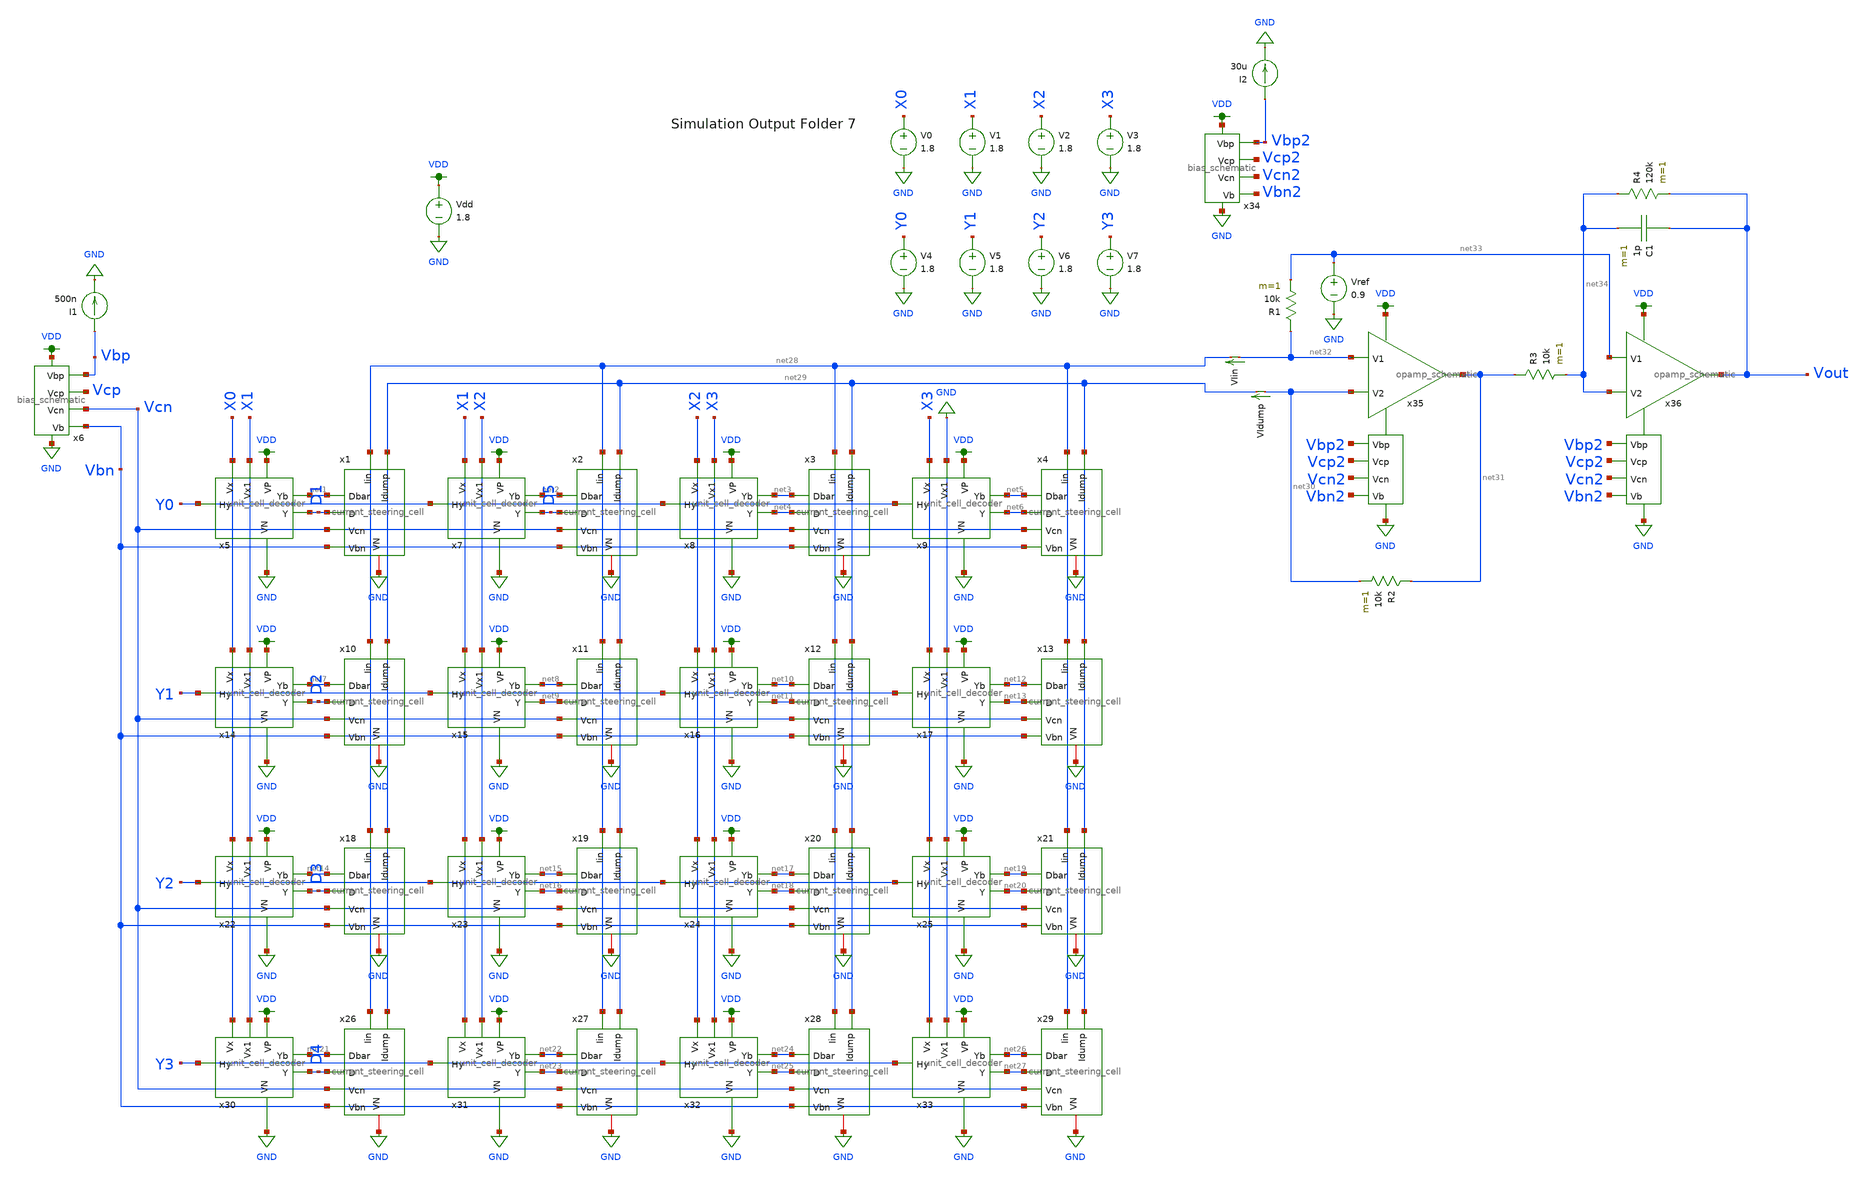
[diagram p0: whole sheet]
** sch_path: xschem/current_steering_testbenches/current_steering_testbench_opamp_iv_2stage_R.sch
**.subckt current_steering_testbench_opamp_iv_2stage_R
V1 X1 GND 1.8
V2 X2 GND 1.8
V3 X3 GND 1.8
V4 Y0 GND 1.8
I1 Vbp GND 500n
Vdd VDD GND 1.8
V5 Y1 GND 1.8
V6 Y2 GND 1.8
V7 Y3 GND 1.8
V0 X0 GND 1.8
x5 X0 X1 Y0 VDD GND net1 D1 unit_cell_decoder
x7 X1 X2 Y0 VDD GND net2 D5 unit_cell_decoder
x8 X2 X3 Y0 VDD GND net3 net4 unit_cell_decoder
x9 X3 GND Y0 VDD GND net5 net6 unit_cell_decoder
x14 X0 X1 Y1 VDD GND net7 D2 unit_cell_decoder
x15 X1 X2 Y1 VDD GND net8 net9 unit_cell_decoder
x16 X2 X3 Y1 VDD GND net10 net11 unit_cell_decoder
x17 X3 GND Y1 VDD GND net12 net13 unit_cell_decoder
x22 X0 X1 Y2 VDD GND net14 D3 unit_cell_decoder
x23 X1 X2 Y2 VDD GND net15 net16 unit_cell_decoder
x24 X2 X3 Y2 VDD GND net17 net18 unit_cell_decoder
x25 X3 GND Y2 VDD GND net19 net20 unit_cell_decoder
x30 X0 X1 Y3 VDD GND net21 D4 unit_cell_decoder
x31 X1 X2 Y3 VDD GND net22 net23 unit_cell_decoder
x32 X2 X3 Y3 VDD GND net24 net25 unit_cell_decoder
x33 X3 GND Y3 VDD GND net26 net27 unit_cell_decoder
x1 net28 net29 net1 D1 Vcn Vbn GND current_steering_cell
x2 net28 net29 net2 D5 Vcn Vbn GND current_steering_cell
x3 net28 net29 net3 net4 Vcn Vbn GND current_steering_cell
x4 net28 net29 net5 net6 Vcn Vbn GND current_steering_cell
x10 net28 net29 net7 D2 Vcn Vbn GND current_steering_cell
x11 net28 net29 net8 net9 Vcn Vbn GND current_steering_cell
x12 net28 net29 net10 net11 Vcn Vbn GND current_steering_cell
x13 net28 net29 net12 net13 Vcn Vbn GND current_steering_cell
x18 net28 net29 net14 D3 Vcn Vbn GND current_steering_cell
x19 net28 net29 net15 net16 Vcn Vbn GND current_steering_cell
x20 net28 net29 net17 net18 Vcn Vbn GND current_steering_cell
x21 net28 net29 net19 net20 Vcn Vbn GND current_steering_cell
x26 net28 net29 net21 D4 Vcn Vbn GND current_steering_cell
x27 net28 net29 net22 net23 Vcn Vbn GND current_steering_cell
x28 net28 net29 net24 net25 Vcn Vbn GND current_steering_cell
x29 net28 net29 net26 net27 Vcn Vbn GND current_steering_cell
x6 VDD Vbp Vcp Vcn GND Vbn bias_schematic
I2 Vbp2 GND 30u
x34 VDD Vbp2 Vcp2 Vcn2 GND Vbn2 bias_schematic
x35 VDD Vbp2 Vcp2 net31 net32 net30 Vcn2 Vbn2 GND opamp_schematic
R1 net32 net33 10k m=1
Vref net33 GND 0.9
R2 net31 net30 10k m=1
VIin net32 net28 0
.save i(viin)
VIdump net30 net29 0
.save i(vidump)
x36 VDD Vbp2 Vcp2 Vout net33 net34 Vcn2 Vbn2 GND opamp_schematic
R3 net31 net34 10k m=1
R4 net34 Vout 120k m=1
C1 Vout net34 1p m=1
**** begin user architecture code

.save all
.control
set wr_vecnames
set wr_singlescale

let mc_runs = 1
let run = 1
dowhile run <= mc_runs

  let code = 0
  while code <= 16

    if code eq 0
      let y0 = 1 * 1.8
      let y1 = 1 * 1.8
      let y2 = 1 * 1.8
      let y3 = 1 * 1.8
      let x0 = 0 * 1.8
      let x1 = 0 * 1.8
      let x2 = 0 * 1.8
      let x3 = 0 * 1.8
    end
    if code eq 1
      let y0 = 1 * 1.8
      let y1 = 0 * 1.8
      let y2 = 0 * 1.8
      let y3 = 0 * 1.8
      let x0 = 1 * 1.8
      let x1 = 0 * 1.8
      let x2 = 0 * 1.8
      let x3 = 0 * 1.8
    end
    if code eq 2
      let y0 = 1 * 1.8
      let y1 = 1 * 1.8
      let y2 = 0 * 1.8
      let y3 = 0 * 1.8
      let x0 = 1 * 1.8
      let x1 = 0 * 1.8
      let x2 = 0 * 1.8
      let x3 = 0 * 1.8
    end
    if code eq 3
      let y0 = 1 * 1.8
      let y1 = 1 * 1.8
      let y2 = 1 * 1.8
      let y3 = 0 * 1.8
      let x0 = 1 * 1.8
      let x1 = 0 * 1.8
      let x2 = 0 * 1.8
      let x3 = 0 * 1.8
    end
    if code eq 4
      let y0 = 1 * 1.8
      let y1 = 1 * 1.8
      let y2 = 1 * 1.8
      let y3 = 1 * 1.8
      let x0 = 1 * 1.8
      let x1 = 0 * 1.8
      let x2 = 0 * 1.8
      let x3 = 0 * 1.8
    end
    if code eq 5
      let y0 = 1 * 1.8
      let y1 = 0 * 1.8
      let y2 = 0 * 1.8
      let y3 = 0 * 1.8
      let x0 = 1 * 1.8
      let x1 = 1 * 1.8
      let x2 = 0 * 1.8
      let x3 = 0 * 1.8
    end
    if code eq 6
      let y0 = 1 * 1.8
      let y1 = 1 * 1.8
      let y2 = 0 * 1.8
      let y3 = 0 * 1.8
      let x0 = 1 * 1.8
      let x1 = 1 * 1.8
      let x2 = 0 * 1.8
      let x3 = 0 * 1.8
    end
    if code eq 7
      let y0 = 1 * 1.8
      let y1 = 1 * 1.8
      let y2 = 1 * 1.8
      let y3 = 0 * 1.8
      let x0 = 1 * 1.8
      let x1 = 1 * 1.8
      let x2 = 0 * 1.8
      let x3 = 0 * 1.8
    end
    if code eq 8
      let y0 = 1 * 1.8
      let y1 = 1 * 1.8
      let y2 = 1 * 1.8
      let y3 = 1 * 1.8
      let x0 = 1 * 1.8
      let x1 = 1 * 1.8
      let x2 = 0 * 1.8
      let x3 = 0 * 1.8
    end
    if code eq 9
      let y0 = 1 * 1.8
      let y1 = 0 * 1.8
      let y2 = 0 * 1.8
      let y3 = 0 * 1.8
      let x0 = 1 * 1.8
      let x1 = 1 * 1.8
      let x2 = 1 * 1.8
      let x3 = 0 * 1.8
    end
    if code eq 10
      let y0 = 1 * 1.8
      let y1 = 1 * 1.8
      let y2 = 0 * 1.8
      let y3 = 0 * 1.8
      let x0 = 1 * 1.8
      let x1 = 1 * 1.8
      let x2 = 1 * 1.8
      let x3 = 0 * 1.8
    end
    if code eq 11
      let y0 = 1 * 1.8
      let y1 = 1 * 1.8
      let y2 = 1 * 1.8
      let y3 = 0 * 1.8
      let x0 = 1 * 1.8
      let x1 = 1 * 1.8
      let x2 = 1 * 1.8
      let x3 = 0 * 1.8
    end
    if code eq 12
      let y0 = 1 * 1.8
      let y1 = 1 * 1.8
      let y2 = 1 * 1.8
      let y3 = 1 * 1.8
      let x0 = 1 * 1.8
      let x1 = 1 * 1.8
      let x2 = 1 * 1.8
      let x3 = 0 * 1.8
    end
    if code eq 13
      let y0 = 1 * 1.8
      let y1 = 0 * 1.8
      let y2 = 0 * 1.8
      let y3 = 0 * 1.8
      let x0 = 1 * 1.8
      let x1 = 1 * 1.8
      let x2 = 1 * 1.8
      let x3 = 1 * 1.8
    end
    if code eq 14
      let y0 = 1 * 1.8
      let y1 = 1 * 1.8
      let y2 = 0 * 1.8
      let y3 = 0 * 1.8
      let x0 = 1 * 1.8
      let x1 = 1 * 1.8
      let x2 = 1 * 1.8
      let x3 = 1 * 1.8
    end
    if code eq 15
      let y0 = 1 * 1.8
      let y1 = 1 * 1.8
      let y2 = 1 * 1.8
      let y3 = 0 * 1.8
      let x0 = 1 * 1.8
      let x1 = 1 * 1.8
      let x2 = 1 * 1.8
      let x3 = 1 * 1.8
    end
    if code eq 16
      let y0 = 1 * 1.8
      let y1 = 1 * 1.8
      let y2 = 1 * 1.8
      let y3 = 1 * 1.8
      let x0 = 1 * 1.8
      let x1 = 1 * 1.8
      let x2 = 1 * 1.8
      let x3 = 1 * 1.8
    end

    alter V0 $&x0
    alter V1 $&x1
    alter V2 $&x2
    alter V3 $&x3
    alter V4 $&y0
    alter V5 $&y1
    alter V6 $&y2
    alter V7 $&y3


    save all
    op

    wrdata ~/dev/git/magic-dds/simulations/current_steering_dac/7/ieeeDAC_{$&run}.txt code v(D1) v(D2)
+ v(D3) v(D4) v(D5) i(VIin) i(VIdump) v(Vout)
    if code eq 0
      set appendwrite
      set wr_vecnames = FALSE
    end
    let code = code + 1
  end
  reset
  set appendwrite = FALSE
  set wr_vecnames
  let run = run + 1
end
.endc


.option wnflag=1
.param MC_SWITCH=0.0
.lib ~/skywater/skywater-pdk/libraries/sky130_fd_pr_ngspice/latest/models/sky130.lib.spice tt

**** end user architecture code
**.ends
.GLOBAL GND
.GLOBAL VDD
.end
